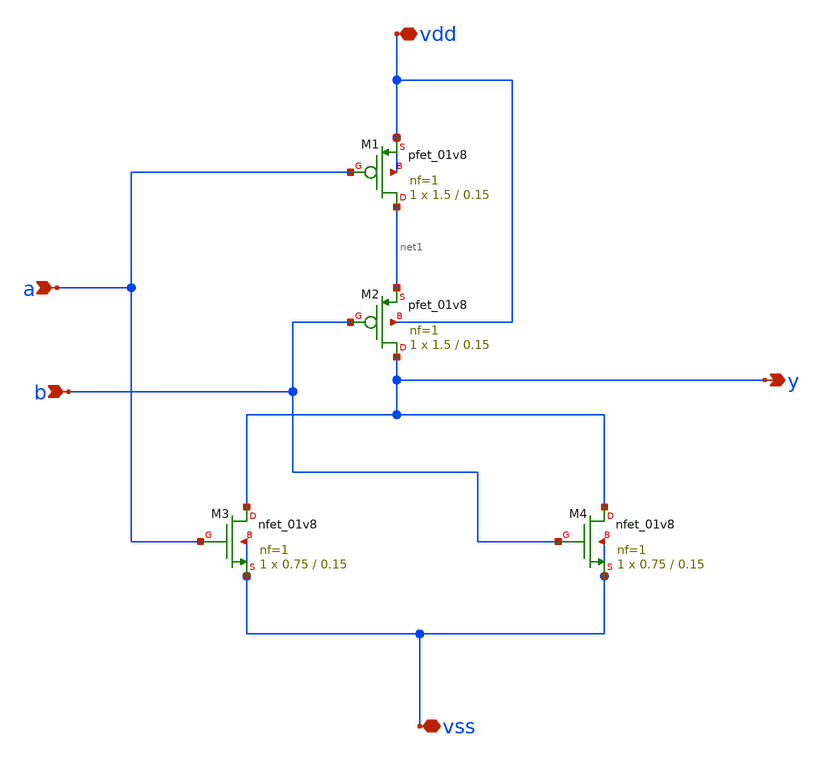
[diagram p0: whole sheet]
** sch_path: xschem/nor_gate.sch
**.subckt nor_gate a b y vdd vss
*.ipin a
*.ipin b
*.opin y
*.iopin vdd
*.iopin vss
XM1 net1 a vdd vdd sky130_fd_pr__pfet_01v8 L=0.15 W=1.5 nf=1 ad='int((nf+1)/2) * W/nf * 0.29' as='int((nf+2)/2) * W/nf * 0.29'
+ pd='2*int((nf+1)/2) * (W/nf + 0.29)' ps='2*int((nf+2)/2) * (W/nf + 0.29)' nrd='0.29 / W' nrs='0.29 / W'
+ sa=0 sb=0 sd=0 mult=1 m=1
XM2 y b net1 vdd sky130_fd_pr__pfet_01v8 L=0.15 W=1.5 nf=1 ad='int((nf+1)/2) * W/nf * 0.29' as='int((nf+2)/2) * W/nf * 0.29'
+ pd='2*int((nf+1)/2) * (W/nf + 0.29)' ps='2*int((nf+2)/2) * (W/nf + 0.29)' nrd='0.29 / W' nrs='0.29 / W'
+ sa=0 sb=0 sd=0 mult=1 m=1
XM3 y a vss vss sky130_fd_pr__nfet_01v8 L=0.15 W=0.75 nf=1 ad='int((nf+1)/2) * W/nf * 0.29' as='int((nf+2)/2) * W/nf * 0.29'
+ pd='2*int((nf+1)/2) * (W/nf + 0.29)' ps='2*int((nf+2)/2) * (W/nf + 0.29)' nrd='0.29 / W' nrs='0.29 / W'
+ sa=0 sb=0 sd=0 mult=1 m=1
XM4 y b vss vss sky130_fd_pr__nfet_01v8 L=0.15 W=0.75 nf=1 ad='int((nf+1)/2) * W/nf * 0.29' as='int((nf+2)/2) * W/nf * 0.29'
+ pd='2*int((nf+1)/2) * (W/nf + 0.29)' ps='2*int((nf+2)/2) * (W/nf + 0.29)' nrd='0.29 / W' nrs='0.29 / W'
+ sa=0 sb=0 sd=0 mult=1 m=1
**.ends
.end
